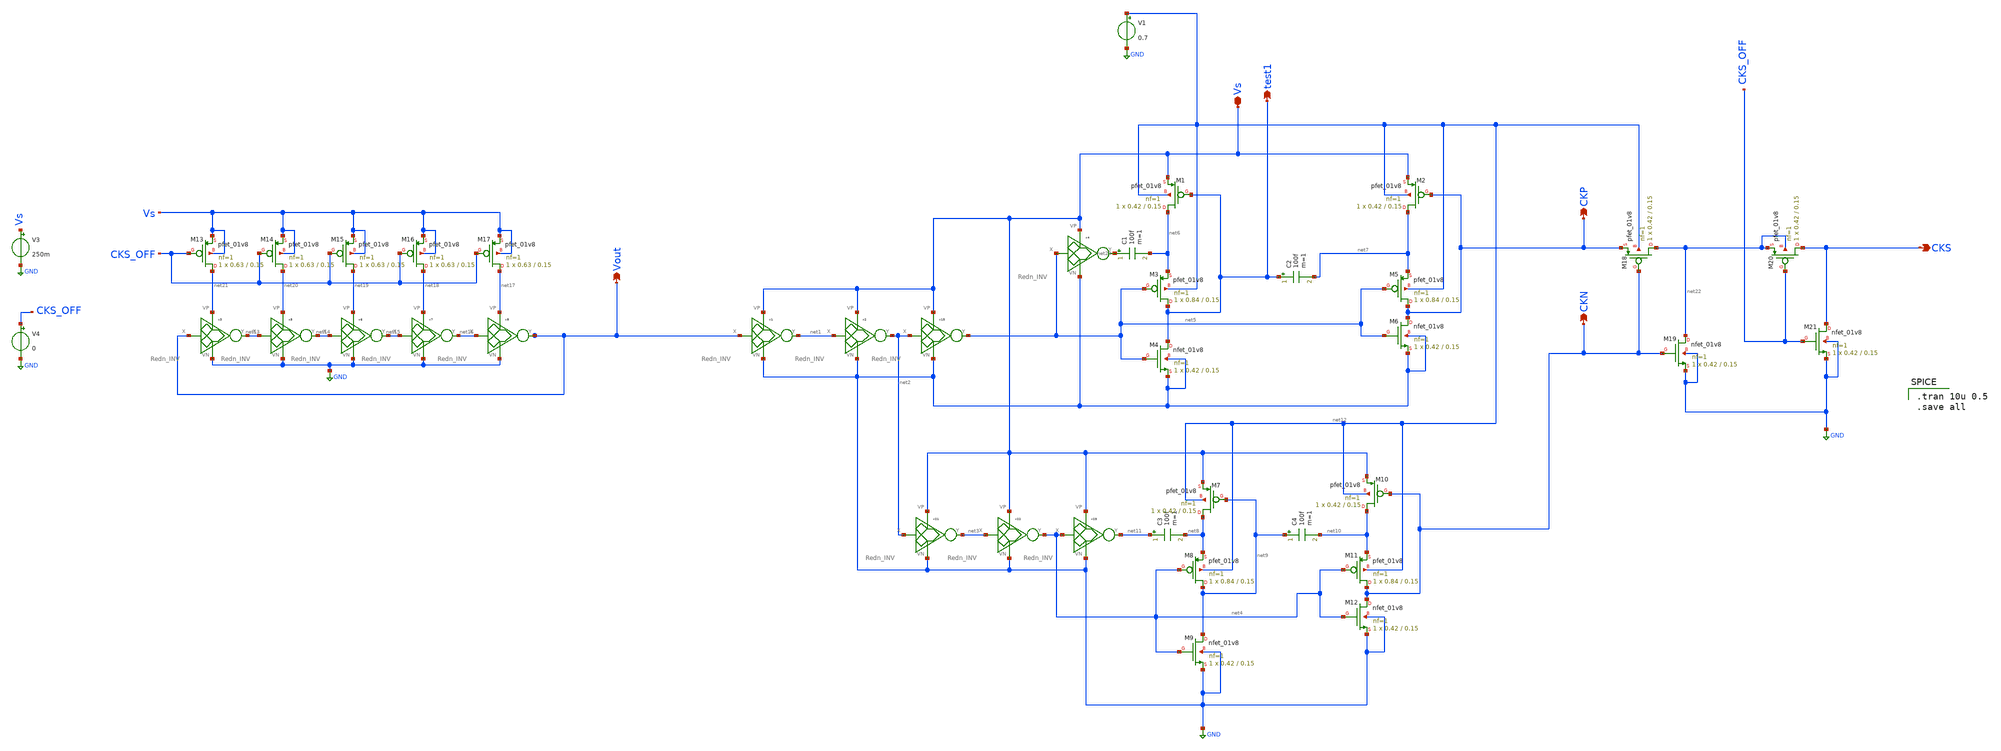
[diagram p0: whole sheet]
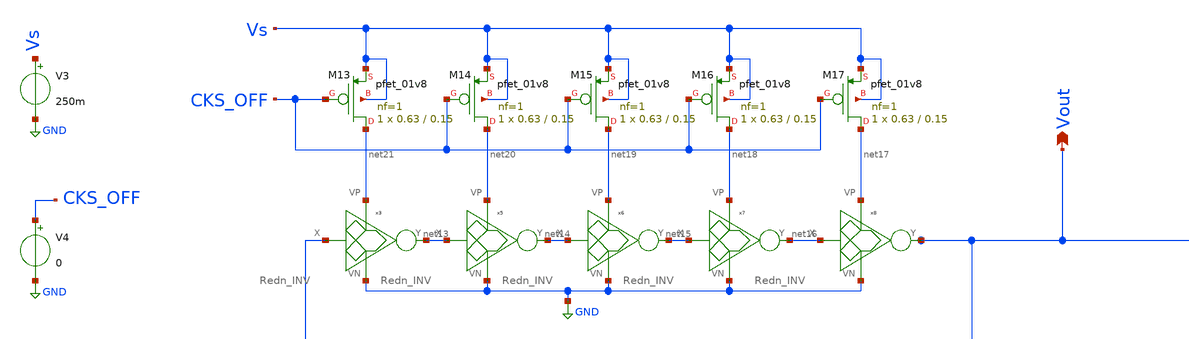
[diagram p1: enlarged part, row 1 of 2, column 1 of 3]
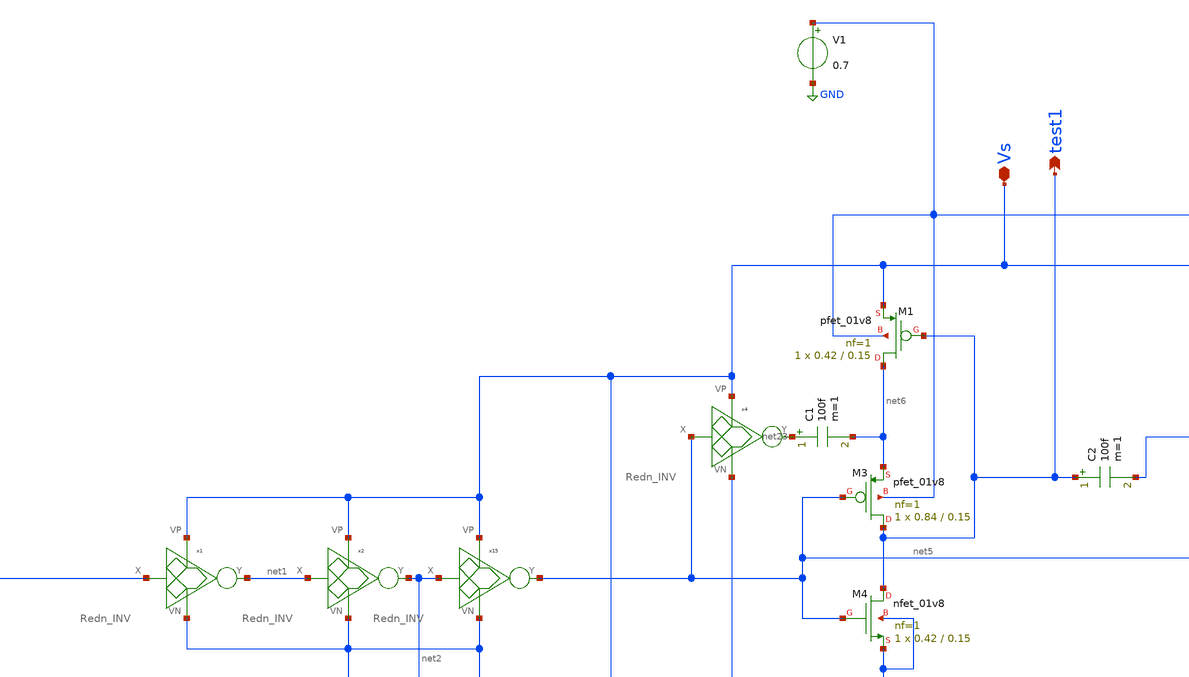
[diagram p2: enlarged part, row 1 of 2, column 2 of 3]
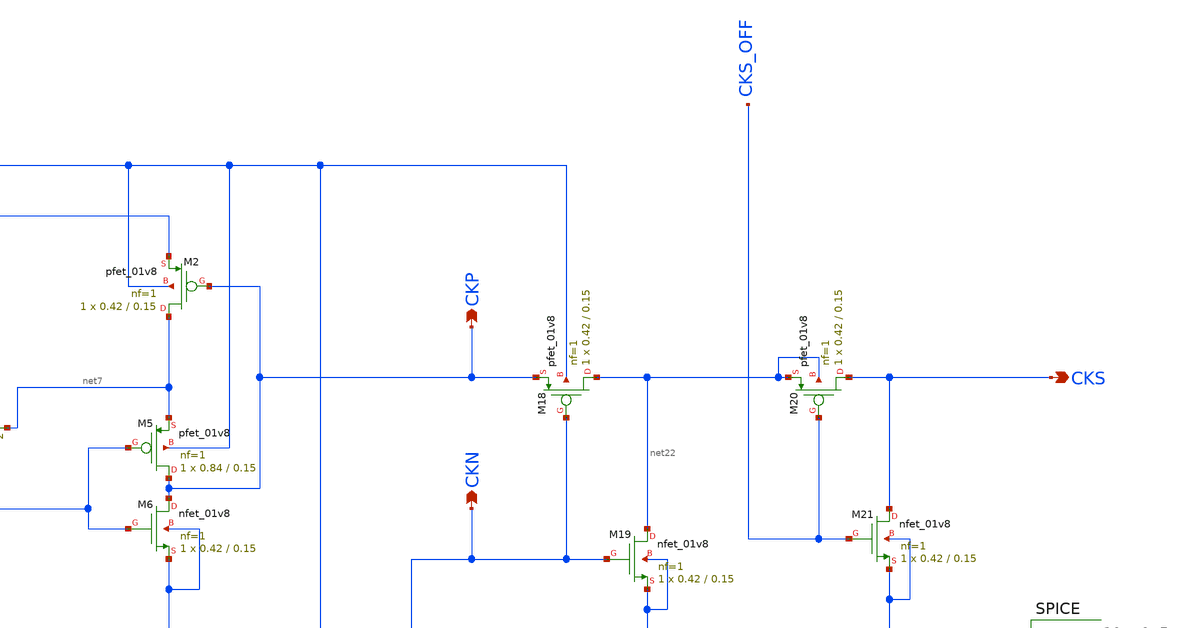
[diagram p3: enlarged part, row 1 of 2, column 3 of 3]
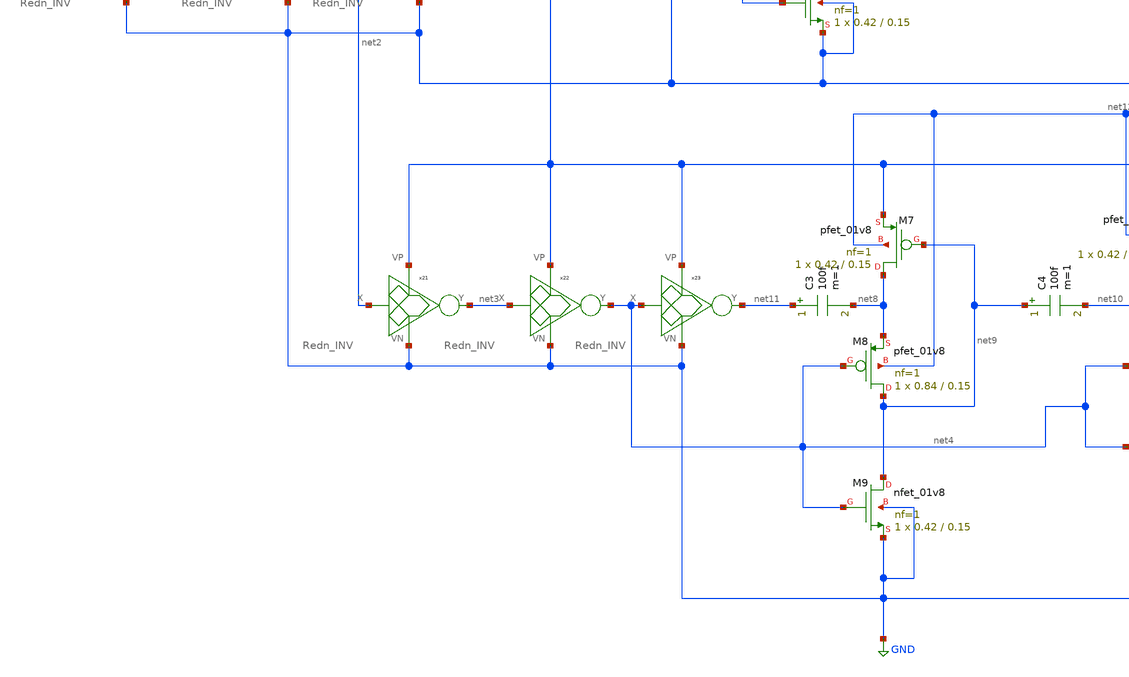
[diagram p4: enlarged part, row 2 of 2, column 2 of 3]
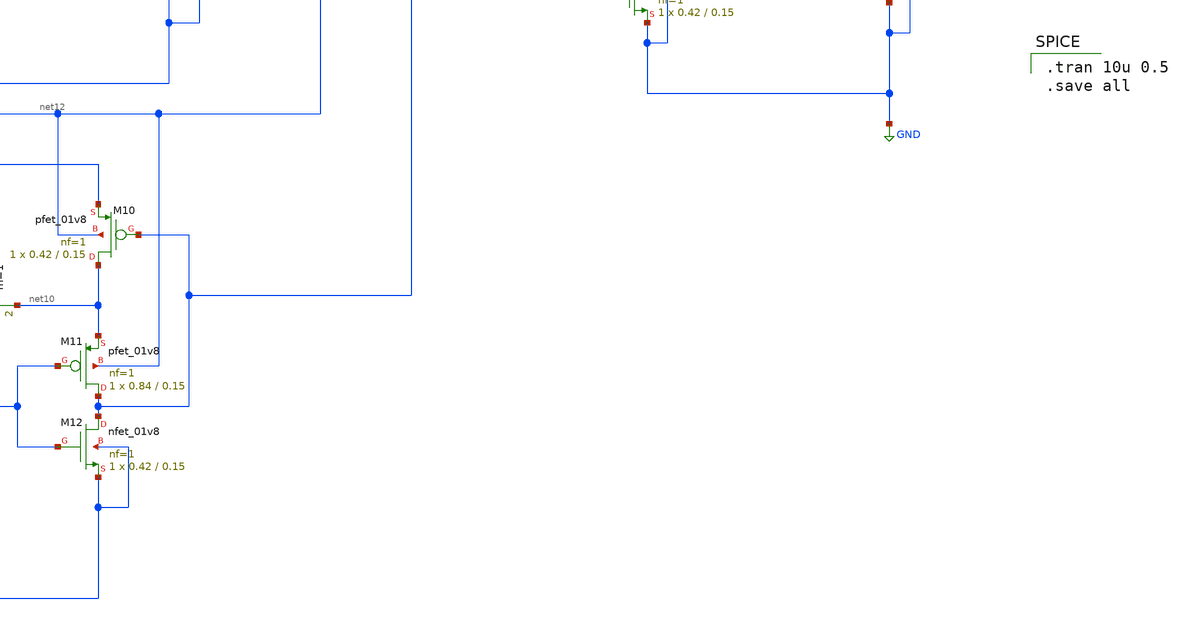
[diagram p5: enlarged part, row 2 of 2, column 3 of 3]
** sch_path: Blocks/StartupConverter/Startup_Converter0.sch
**.subckt Startup_Converter0 CKP CKN Vout Vs CKS test1
*.opin CKP
*.opin CKN
*.opin Vout
*.iopin Vs
*.opin CKS
*.opin test1
C1 net23 net6 100f m=1
XM1 net6 test1 Vs net12 sky130_fd_pr__pfet_01v8 L=0.15 W=0.42 nf=1 ad='int((nf+1)/2) * W/nf * 0.29' as='int((nf+2)/2) * W/nf * 0.29'
+ pd='2*int((nf+1)/2) * (W/nf + 0.29)' ps='2*int((nf+2)/2) * (W/nf + 0.29)' nrd='0.29 / W' nrs='0.29 / W'
+ sa=0 sb=0 sd=0 mult=1 m=1
XM3 test1 net5 net6 net12 sky130_fd_pr__pfet_01v8 L=0.15 W=0.84 nf=1 ad='int((nf+1)/2) * W/nf * 0.29'
+ as='int((nf+2)/2) * W/nf * 0.29' pd='2*int((nf+1)/2) * (W/nf + 0.29)' ps='2*int((nf+2)/2) * (W/nf + 0.29)'
+ nrd='0.29 / W' nrs='0.29 / W' sa=0 sb=0 sd=0 mult=1 m=1
XM4 test1 net5 GND GND sky130_fd_pr__nfet_01v8 L=0.15 W=0.42 nf=1 ad='int((nf+1)/2) * W/nf * 0.29' as='int((nf+2)/2) * W/nf * 0.29'
+ pd='2*int((nf+1)/2) * (W/nf + 0.29)' ps='2*int((nf+2)/2) * (W/nf + 0.29)' nrd='0.29 / W' nrs='0.29 / W'
+ sa=0 sb=0 sd=0 mult=1 m=1
XM2 net7 CKP Vs net12 sky130_fd_pr__pfet_01v8 L=0.15 W=0.42 nf=1 ad='int((nf+1)/2) * W/nf * 0.29' as='int((nf+2)/2) * W/nf * 0.29'
+ pd='2*int((nf+1)/2) * (W/nf + 0.29)' ps='2*int((nf+2)/2) * (W/nf + 0.29)' nrd='0.29 / W' nrs='0.29 / W'
+ sa=0 sb=0 sd=0 mult=1 m=1
XM5 CKP net5 net7 net12 sky130_fd_pr__pfet_01v8 L=0.15 W=0.84 nf=1 ad='int((nf+1)/2) * W/nf * 0.29' as='int((nf+2)/2) * W/nf * 0.29'
+ pd='2*int((nf+1)/2) * (W/nf + 0.29)' ps='2*int((nf+2)/2) * (W/nf + 0.29)' nrd='0.29 / W' nrs='0.29 / W'
+ sa=0 sb=0 sd=0 mult=1 m=1
XM6 CKP net5 GND GND sky130_fd_pr__nfet_01v8 L=0.15 W=0.42 nf=1 ad='int((nf+1)/2) * W/nf * 0.29' as='int((nf+2)/2) * W/nf * 0.29'
+ pd='2*int((nf+1)/2) * (W/nf + 0.29)' ps='2*int((nf+2)/2) * (W/nf + 0.29)' nrd='0.29 / W' nrs='0.29 / W'
+ sa=0 sb=0 sd=0 mult=1 m=1
C3 net11 net8 100f m=1
XM8 net9 net4 net8 net12 sky130_fd_pr__pfet_01v8 L=0.15 W=0.84 nf=1 ad='int((nf+1)/2) * W/nf * 0.29'
+ as='int((nf+2)/2) * W/nf * 0.29' pd='2*int((nf+1)/2) * (W/nf + 0.29)' ps='2*int((nf+2)/2) * (W/nf + 0.29)'
+ nrd='0.29 / W' nrs='0.29 / W' sa=0 sb=0 sd=0 mult=1 m=1
XM9 net9 net4 GND GND sky130_fd_pr__nfet_01v8 L=0.15 W=0.42 nf=1 ad='int((nf+1)/2) * W/nf * 0.29' as='int((nf+2)/2) * W/nf * 0.29'
+ pd='2*int((nf+1)/2) * (W/nf + 0.29)' ps='2*int((nf+2)/2) * (W/nf + 0.29)' nrd='0.29 / W' nrs='0.29 / W'
+ sa=0 sb=0 sd=0 mult=1 m=1
XM10 net10 CKN Vs net12 sky130_fd_pr__pfet_01v8 L=0.15 W=0.42 nf=1 ad='int((nf+1)/2) * W/nf * 0.29' as='int((nf+2)/2) * W/nf * 0.29'
+ pd='2*int((nf+1)/2) * (W/nf + 0.29)' ps='2*int((nf+2)/2) * (W/nf + 0.29)' nrd='0.29 / W' nrs='0.29 / W'
+ sa=0 sb=0 sd=0 mult=1 m=1
XM11 CKN net4 net10 net12 sky130_fd_pr__pfet_01v8 L=0.15 W=0.84 nf=1 ad='int((nf+1)/2) * W/nf * 0.29'
+ as='int((nf+2)/2) * W/nf * 0.29' pd='2*int((nf+1)/2) * (W/nf + 0.29)' ps='2*int((nf+2)/2) * (W/nf + 0.29)'
+ nrd='0.29 / W' nrs='0.29 / W' sa=0 sb=0 sd=0 mult=1 m=1
XM12 CKN net4 GND GND sky130_fd_pr__nfet_01v8 L=0.15 W=0.42 nf=1 ad='int((nf+1)/2) * W/nf * 0.29' as='int((nf+2)/2) * W/nf * 0.29'
+ pd='2*int((nf+1)/2) * (W/nf + 0.29)' ps='2*int((nf+2)/2) * (W/nf + 0.29)' nrd='0.29 / W' nrs='0.29 / W'
+ sa=0 sb=0 sd=0 mult=1 m=1
C4 net9 net10 100f m=1
XM7 net8 net9 Vs net12 sky130_fd_pr__pfet_01v8 L=0.15 W=0.42 nf=1 ad='int((nf+1)/2) * W/nf * 0.29' as='int((nf+2)/2) * W/nf * 0.29'
+ pd='2*int((nf+1)/2) * (W/nf + 0.29)' ps='2*int((nf+2)/2) * (W/nf + 0.29)' nrd='0.29 / W' nrs='0.29 / W'
+ sa=0 sb=0 sd=0 mult=1 m=1
x4 net5 net23 Vs GND Redn_INV
x1 Vout net1 Vs GND Redn_INV
x2 net1 net2 Vs GND Redn_INV
x15 net2 net5 Vs GND Redn_INV
x21 net2 net3 Vs GND Redn_INV
x22 net3 net4 Vs GND Redn_INV
x23 net4 net11 Vs GND Redn_INV
V3 Vs GND 250m
x3 Vout net13 net21 GND Redn_INV
x5 net13 net14 net20 GND Redn_INV
x6 net14 net15 net19 GND Redn_INV
x7 net15 net16 net18 GND Redn_INV
x8 net16 Vout net17 GND Redn_INV
XM13 net21 CKS_OFF Vs Vs sky130_fd_pr__pfet_01v8 L=0.15 W=0.63 nf=1 ad='int((nf+1)/2) * W/nf * 0.29'
+ as='int((nf+2)/2) * W/nf * 0.29' pd='2*int((nf+1)/2) * (W/nf + 0.29)' ps='2*int((nf+2)/2) * (W/nf + 0.29)'
+ nrd='0.29 / W' nrs='0.29 / W' sa=0 sb=0 sd=0 mult=1 m=1
XM14 net20 CKS_OFF Vs Vs sky130_fd_pr__pfet_01v8 L=0.15 W=0.63 nf=1 ad='int((nf+1)/2) * W/nf * 0.29'
+ as='int((nf+2)/2) * W/nf * 0.29' pd='2*int((nf+1)/2) * (W/nf + 0.29)' ps='2*int((nf+2)/2) * (W/nf + 0.29)'
+ nrd='0.29 / W' nrs='0.29 / W' sa=0 sb=0 sd=0 mult=1 m=1
XM15 net19 CKS_OFF Vs Vs sky130_fd_pr__pfet_01v8 L=0.15 W=0.63 nf=1 ad='int((nf+1)/2) * W/nf * 0.29'
+ as='int((nf+2)/2) * W/nf * 0.29' pd='2*int((nf+1)/2) * (W/nf + 0.29)' ps='2*int((nf+2)/2) * (W/nf + 0.29)'
+ nrd='0.29 / W' nrs='0.29 / W' sa=0 sb=0 sd=0 mult=1 m=1
XM16 net18 CKS_OFF Vs Vs sky130_fd_pr__pfet_01v8 L=0.15 W=0.63 nf=1 ad='int((nf+1)/2) * W/nf * 0.29'
+ as='int((nf+2)/2) * W/nf * 0.29' pd='2*int((nf+1)/2) * (W/nf + 0.29)' ps='2*int((nf+2)/2) * (W/nf + 0.29)'
+ nrd='0.29 / W' nrs='0.29 / W' sa=0 sb=0 sd=0 mult=1 m=1
XM17 net17 CKS_OFF Vs Vs sky130_fd_pr__pfet_01v8 L=0.15 W=0.63 nf=1 ad='int((nf+1)/2) * W/nf * 0.29'
+ as='int((nf+2)/2) * W/nf * 0.29' pd='2*int((nf+1)/2) * (W/nf + 0.29)' ps='2*int((nf+2)/2) * (W/nf + 0.29)'
+ nrd='0.29 / W' nrs='0.29 / W' sa=0 sb=0 sd=0 mult=1 m=1
V4 CKS_OFF GND 0
V1 net12 GND 0.7
C2 test1 net7 100f m=1
XM18 net22 CKN CKP net12 sky130_fd_pr__pfet_01v8 L=0.15 W=0.42 nf=1 ad='int((nf+1)/2) * W/nf * 0.29'
+ as='int((nf+2)/2) * W/nf * 0.29' pd='2*int((nf+1)/2) * (W/nf + 0.29)' ps='2*int((nf+2)/2) * (W/nf + 0.29)'
+ nrd='0.29 / W' nrs='0.29 / W' sa=0 sb=0 sd=0 mult=1 m=1
XM19 net22 CKN GND GND sky130_fd_pr__nfet_01v8 L=0.15 W=0.42 nf=1 ad='int((nf+1)/2) * W/nf * 0.29' as='int((nf+2)/2) * W/nf * 0.29'
+ pd='2*int((nf+1)/2) * (W/nf + 0.29)' ps='2*int((nf+2)/2) * (W/nf + 0.29)' nrd='0.29 / W' nrs='0.29 / W'
+ sa=0 sb=0 sd=0 mult=1 m=1
XM21 CKS CKS_OFF GND GND sky130_fd_pr__nfet_01v8 L=0.15 W=0.42 nf=1 ad='int((nf+1)/2) * W/nf * 0.29'
+ as='int((nf+2)/2) * W/nf * 0.29' pd='2*int((nf+1)/2) * (W/nf + 0.29)' ps='2*int((nf+2)/2) * (W/nf + 0.29)'
+ nrd='0.29 / W' nrs='0.29 / W' sa=0 sb=0 sd=0 mult=1 m=1
XM20 CKS CKS_OFF net22 net22 sky130_fd_pr__pfet_01v8 L=0.15 W=0.42 nf=1 ad='int((nf+1)/2) * W/nf * 0.29'
+ as='int((nf+2)/2) * W/nf * 0.29' pd='2*int((nf+1)/2) * (W/nf + 0.29)' ps='2*int((nf+2)/2) * (W/nf + 0.29)'
+ nrd='0.29 / W' nrs='0.29 / W' sa=0 sb=0 sd=0 mult=1 m=1
**** begin user architecture code

** opencircuitdesign pdks install
.lib $::SKYWATER_MODELS/sky130.lib.spice tt



.tran 10u 0.5
.save all

**** end user architecture code
**.ends

* expanding   symbol:  Pico_project/Rdn_INV/Redn_INV.sym # of pins=4
** sym_path: component/Reduntant_Inverter/Redn_INV.sym
** sch_path: component/Reduntant_Inverter/Redn_INV.sch
.subckt Redn_INV X Y VP VN
*.opin Y
*.ipin X
*.iopin VP
*.iopin VN
XM15 net4 X VN VN sky130_fd_pr__nfet_01v8_lvt L=0.15 W=1 nf=1 ad='int((nf+1)/2) * W/nf * 0.29' as='int((nf+2)/2) * W/nf * 0.29'
+ pd='2*int((nf+1)/2) * (W/nf + 0.29)' ps='2*int((nf+2)/2) * (W/nf + 0.29)' nrd='0.29 / W' nrs='0.29 / W'
+ sa=0 sb=0 sd=0 mult=1 m=1
XM1 net5 X net3 VN sky130_fd_pr__nfet_01v8_lvt L=0.15 W=3.25 nf=1 ad='int((nf+1)/2) * W/nf * 0.29' as='int((nf+2)/2) * W/nf * 0.29'
+ pd='2*int((nf+1)/2) * (W/nf + 0.29)' ps='2*int((nf+2)/2) * (W/nf + 0.29)' nrd='0.29 / W' nrs='0.29 / W'
+ sa=0 sb=0 sd=0 mult=1 m=1
XM16 Y X net6 VN sky130_fd_pr__nfet_01v8_lvt L=0.15 W=6.5 nf=1 ad='int((nf+1)/2) * W/nf * 0.29' as='int((nf+2)/2) * W/nf * 0.29'
+ pd='2*int((nf+1)/2) * (W/nf + 0.29)' ps='2*int((nf+2)/2) * (W/nf + 0.29)' nrd='0.29 / W' nrs='0.29 / W'
+ sa=0 sb=0 sd=0 mult=1 m=1
XM17 net3 X VN VN sky130_fd_pr__nfet_01v8_lvt L=0.15 W=3.25 nf=1 ad='int((nf+1)/2) * W/nf * 0.29' as='int((nf+2)/2) * W/nf * 0.29'
+ pd='2*int((nf+1)/2) * (W/nf + 0.29)' ps='2*int((nf+2)/2) * (W/nf + 0.29)' nrd='0.29 / W' nrs='0.29 / W'
+ sa=0 sb=0 sd=0 mult=1 m=1
XM18 net2 X VN VN sky130_fd_pr__nfet_01v8_lvt L=0.15 W=1.5 nf=1 ad='int((nf+1)/2) * W/nf * 0.29' as='int((nf+2)/2) * W/nf * 0.29'
+ pd='2*int((nf+1)/2) * (W/nf + 0.29)' ps='2*int((nf+2)/2) * (W/nf + 0.29)' nrd='0.29 / W' nrs='0.29 / W'
+ sa=0 sb=0 sd=0 mult=1 m=1
XM19 net1 X VN VN sky130_fd_pr__nfet_01v8_lvt L=0.15 W=6.5 nf=1 ad='int((nf+1)/2) * W/nf * 0.29' as='int((nf+2)/2) * W/nf * 0.29'
+ pd='2*int((nf+1)/2) * (W/nf + 0.29)' ps='2*int((nf+2)/2) * (W/nf + 0.29)' nrd='0.29 / W' nrs='0.29 / W'
+ sa=0 sb=0 sd=0 mult=1 m=1
XM20 net6 X net1 VN sky130_fd_pr__nfet_01v8_lvt L=0.15 W=6.5 nf=1 ad='int((nf+1)/2) * W/nf * 0.29' as='int((nf+2)/2) * W/nf * 0.29'
+ pd='2*int((nf+1)/2) * (W/nf + 0.29)' ps='2*int((nf+2)/2) * (W/nf + 0.29)' nrd='0.29 / W' nrs='0.29 / W'
+ sa=0 sb=0 sd=0 mult=1 m=1
XM2 net4 X VP VP sky130_fd_pr__pfet_01v8 L=0.15 W=10 nf=1 ad='int((nf+1)/2) * W/nf * 0.29' as='int((nf+2)/2) * W/nf * 0.29'
+ pd='2*int((nf+1)/2) * (W/nf + 0.29)' ps='2*int((nf+2)/2) * (W/nf + 0.29)' nrd='0.29 / W' nrs='0.29 / W'
+ sa=0 sb=0 sd=0 mult=1 m=1
XM5 net5 X net4 net4 sky130_fd_pr__pfet_01v8 L=0.15 W=10 nf=1 ad='int((nf+1)/2) * W/nf * 0.29' as='int((nf+2)/2) * W/nf * 0.29'
+ pd='2*int((nf+1)/2) * (W/nf + 0.29)' ps='2*int((nf+2)/2) * (W/nf + 0.29)' nrd='0.29 / W' nrs='0.29 / W'
+ sa=0 sb=0 sd=0 mult=1 m=1
XM6 Y X net5 VP sky130_fd_pr__pfet_01v8 L=0.15 W=10 nf=1 ad='int((nf+1)/2) * W/nf * 0.29' as='int((nf+2)/2) * W/nf * 0.29'
+ pd='2*int((nf+1)/2) * (W/nf + 0.29)' ps='2*int((nf+2)/2) * (W/nf + 0.29)' nrd='0.29 / W' nrs='0.29 / W'
+ sa=0 sb=0 sd=0 mult=1 m=1
XM8 net3 X VP VP sky130_fd_pr__pfet_01v8 L=0.15 W=2 nf=1 ad='int((nf+1)/2) * W/nf * 0.29' as='int((nf+2)/2) * W/nf * 0.29'
+ pd='2*int((nf+1)/2) * (W/nf + 0.29)' ps='2*int((nf+2)/2) * (W/nf + 0.29)' nrd='0.29 / W' nrs='0.29 / W'
+ sa=0 sb=0 sd=0 mult=1 m=1
XM12 net2 X VP VP sky130_fd_pr__pfet_01v8 L=0.15 W=5 nf=1 ad='int((nf+1)/2) * W/nf * 0.29' as='int((nf+2)/2) * W/nf * 0.29'
+ pd='2*int((nf+1)/2) * (W/nf + 0.29)' ps='2*int((nf+2)/2) * (W/nf + 0.29)' nrd='0.29 / W' nrs='0.29 / W'
+ sa=0 sb=0 sd=0 mult=1 m=1
XM14 net6 X net2 VP sky130_fd_pr__pfet_01v8 L=0.15 W=5 nf=1 ad='int((nf+1)/2) * W/nf * 0.29' as='int((nf+2)/2) * W/nf * 0.29'
+ pd='2*int((nf+1)/2) * (W/nf + 0.29)' ps='2*int((nf+2)/2) * (W/nf + 0.29)' nrd='0.29 / W' nrs='0.29 / W'
+ sa=0 sb=0 sd=0 mult=1 m=1
XM21 net1 X VP VP sky130_fd_pr__pfet_01v8 L=0.15 W=1.5 nf=1 ad='int((nf+1)/2) * W/nf * 0.29' as='int((nf+2)/2) * W/nf * 0.29'
+ pd='2*int((nf+1)/2) * (W/nf + 0.29)' ps='2*int((nf+2)/2) * (W/nf + 0.29)' nrd='0.29 / W' nrs='0.29 / W'
+ sa=0 sb=0 sd=0 mult=1 m=1
.ends

.GLOBAL GND
.end
